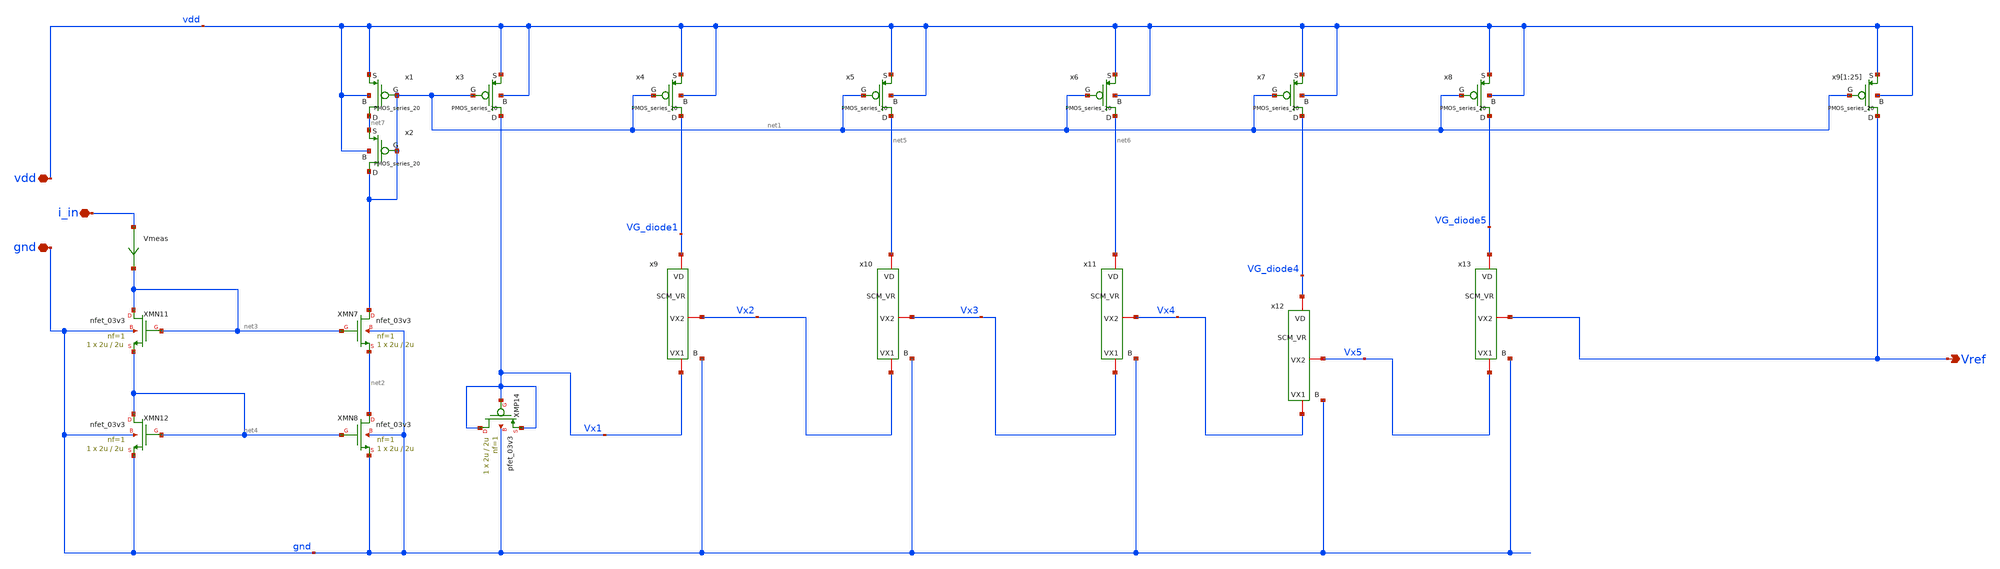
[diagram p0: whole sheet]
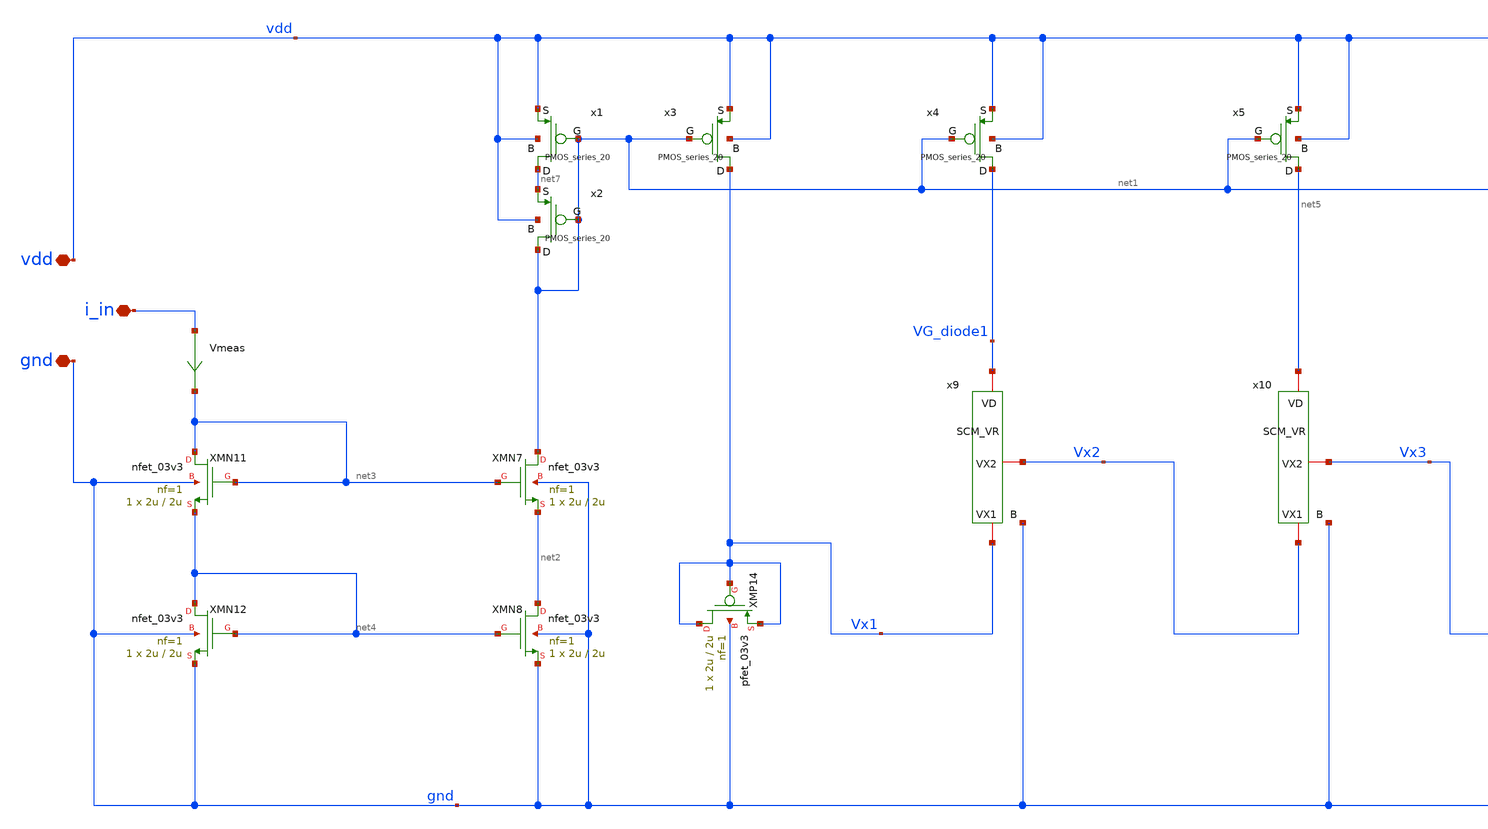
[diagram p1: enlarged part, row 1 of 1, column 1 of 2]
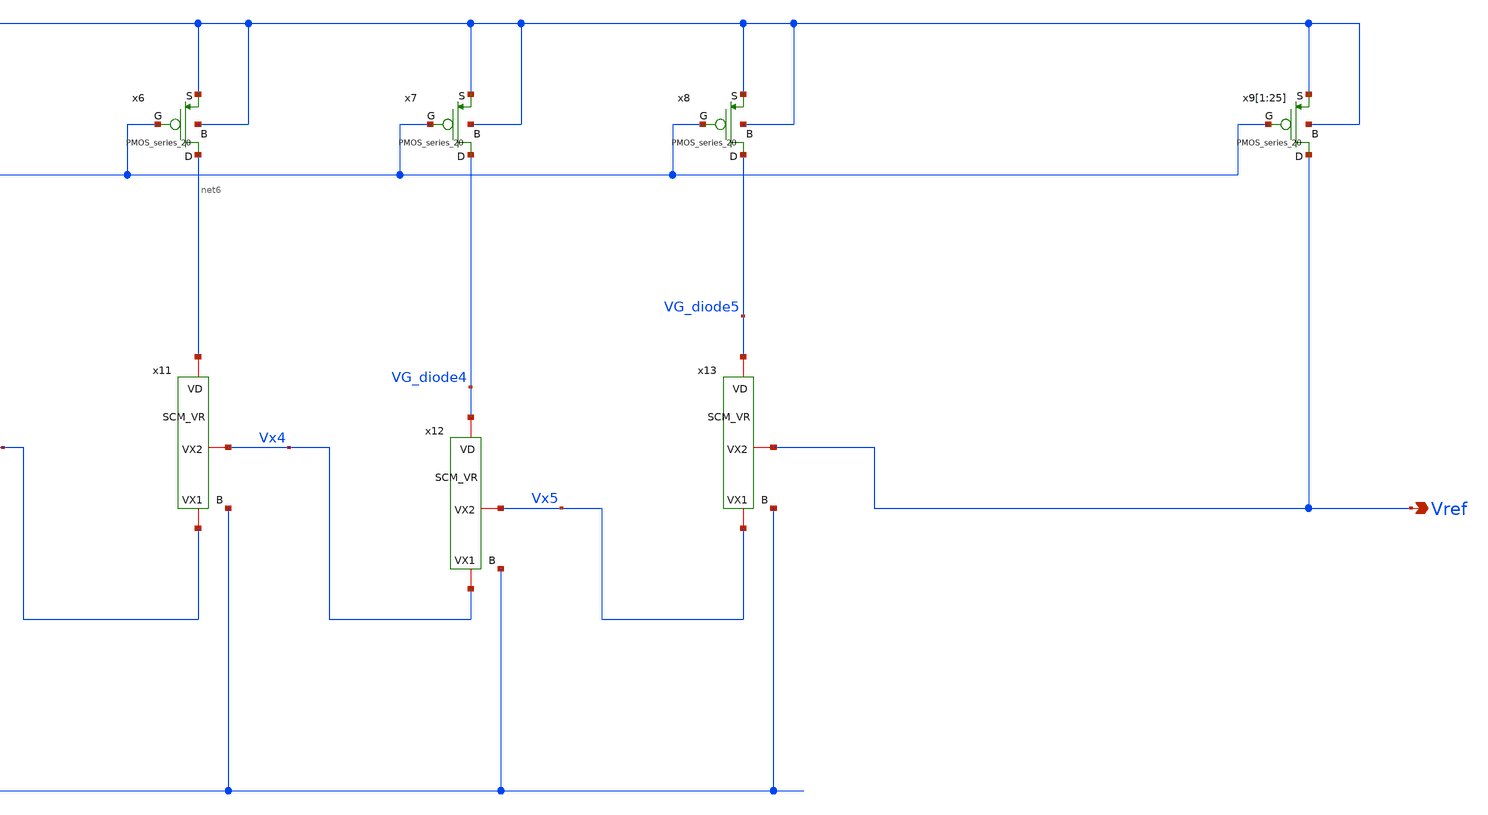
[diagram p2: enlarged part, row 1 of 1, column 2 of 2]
** sch_path: Voltage_Reference/symbols_vr/Voltege_Reference.sch
**.subckt Voltege_Reference i_in vdd gnd Vref
*.iopin i_in
*.iopin vdd
*.iopin gnd
*.opin Vref
XMN7 net1 net3 net2 gnd nfet_03v3 L=2u W=2u nf=1 ad='int((nf+1)/2) * W/nf * 0.18u' as='int((nf+2)/2) * W/nf * 0.18u'
+ pd='2*int((nf+1)/2) * (W/nf + 0.18u)' ps='2*int((nf+2)/2) * (W/nf + 0.18u)' nrd='0.18u / W' nrs='0.18u / W'
+ sa=0 sb=0 sd=0 m=1
XMN8 net2 net4 gnd gnd nfet_03v3 L=2u W=2u nf=1 ad='int((nf+1)/2) * W/nf * 0.18u' as='int((nf+2)/2) * W/nf * 0.18u'
+ pd='2*int((nf+1)/2) * (W/nf + 0.18u)' ps='2*int((nf+2)/2) * (W/nf + 0.18u)' nrd='0.18u / W' nrs='0.18u / W'
+ sa=0 sb=0 sd=0 m=1
XMP14 Vx1 Vx1 Vx1 gnd pfet_03v3 L=2u W=2u nf=1 ad='int((nf+1)/2) * W/nf * 0.18u' as='int((nf+2)/2) * W/nf * 0.18u'
+ pd='2*int((nf+1)/2) * (W/nf + 0.18u)' ps='2*int((nf+2)/2) * (W/nf + 0.18u)' nrd='0.18u / W' nrs='0.18u / W'
+ sa=0 sb=0 sd=0 m=1
XMN11 net3 net3 net4 gnd nfet_03v3 L=2u W=2u nf=1 ad='int((nf+1)/2) * W/nf * 0.18u' as='int((nf+2)/2) * W/nf * 0.18u'
+ pd='2*int((nf+1)/2) * (W/nf + 0.18u)' ps='2*int((nf+2)/2) * (W/nf + 0.18u)' nrd='0.18u / W' nrs='0.18u / W'
+ sa=0 sb=0 sd=0 m=1
XMN12 net4 net4 gnd gnd nfet_03v3 L=2u W=2u nf=1 ad='int((nf+1)/2) * W/nf * 0.18u' as='int((nf+2)/2) * W/nf * 0.18u'
+ pd='2*int((nf+1)/2) * (W/nf + 0.18u)' ps='2*int((nf+2)/2) * (W/nf + 0.18u)' nrd='0.18u / W' nrs='0.18u / W'
+ sa=0 sb=0 sd=0 m=1
Vmeas i_in net3 0
.save i(vmeas)
x1 vdd net7 vdd net1 PMOS_series_20
x2 net7 net1 vdd net1 PMOS_series_20
x3 vdd Vx1 vdd net1 PMOS_series_20
x4 vdd VG_diode1 vdd net1 PMOS_series_20
x5 vdd net5 vdd net1 PMOS_series_20
x6 vdd net6 vdd net1 PMOS_series_20
x7 vdd VG_diode4 vdd net1 PMOS_series_20
x8 vdd VG_diode5 vdd net1 PMOS_series_20
x9[1] vdd Vref vdd net1 PMOS_series_20
x9[2] vdd Vref vdd net1 PMOS_series_20
x9[3] vdd Vref vdd net1 PMOS_series_20
x9[4] vdd Vref vdd net1 PMOS_series_20
x9[5] vdd Vref vdd net1 PMOS_series_20
x9[6] vdd Vref vdd net1 PMOS_series_20
x9[7] vdd Vref vdd net1 PMOS_series_20
x9[8] vdd Vref vdd net1 PMOS_series_20
x9[9] vdd Vref vdd net1 PMOS_series_20
x9[10] vdd Vref vdd net1 PMOS_series_20
x9[11] vdd Vref vdd net1 PMOS_series_20
x9[12] vdd Vref vdd net1 PMOS_series_20
x9[13] vdd Vref vdd net1 PMOS_series_20
x9[14] vdd Vref vdd net1 PMOS_series_20
x9[15] vdd Vref vdd net1 PMOS_series_20
x9[16] vdd Vref vdd net1 PMOS_series_20
x9[17] vdd Vref vdd net1 PMOS_series_20
x9[18] vdd Vref vdd net1 PMOS_series_20
x9[19] vdd Vref vdd net1 PMOS_series_20
x9[20] vdd Vref vdd net1 PMOS_series_20
x9[21] vdd Vref vdd net1 PMOS_series_20
x9[22] vdd Vref vdd net1 PMOS_series_20
x9[23] vdd Vref vdd net1 PMOS_series_20
x9[24] vdd Vref vdd net1 PMOS_series_20
x9[25] vdd Vref vdd net1 PMOS_series_20
x9 VG_diode1 Vx1 Vx2 gnd SCM_VR
x10 net5 Vx2 Vx3 gnd SCM_VR
x11 net6 Vx3 Vx4 gnd SCM_VR
x12 VG_diode4 Vx4 Vx5 gnd SCM_VR
x13 VG_diode5 Vx5 Vref gnd SCM_VR
**.ends

* expanding   symbol:  symbols_vr/PMOS_series_20.sym # of pins=4
** sym_path: Voltage_Reference/symbols_vr/PMOS_series_20.sym
** sch_path: Voltage_Reference/symbols_vr/PMOS_series_20.sch
.subckt PMOS_series_20 S D B G
*.iopin S
*.iopin D
*.iopin B
*.iopin G
XMP1 net1 G S B pfet_03v3 L=2u W=2u nf=1 ad='int((nf+1)/2) * W/nf * 0.18u' as='int((nf+2)/2) * W/nf * 0.18u'
+ pd='2*int((nf+1)/2) * (W/nf + 0.18u)' ps='2*int((nf+2)/2) * (W/nf + 0.18u)' nrd='0.18u / W' nrs='0.18u / W'
+ sa=0 sb=0 sd=0 m=1
XMP2 net3 G net1 B pfet_03v3 L=2u W=2u nf=1 ad='int((nf+1)/2) * W/nf * 0.18u' as='int((nf+2)/2) * W/nf * 0.18u'
+ pd='2*int((nf+1)/2) * (W/nf + 0.18u)' ps='2*int((nf+2)/2) * (W/nf + 0.18u)' nrd='0.18u / W' nrs='0.18u / W'
+ sa=0 sb=0 sd=0 m=1
XMP3 net2 G net3 B pfet_03v3 L=2u W=2u nf=1 ad='int((nf+1)/2) * W/nf * 0.18u' as='int((nf+2)/2) * W/nf * 0.18u'
+ pd='2*int((nf+1)/2) * (W/nf + 0.18u)' ps='2*int((nf+2)/2) * (W/nf + 0.18u)' nrd='0.18u / W' nrs='0.18u / W'
+ sa=0 sb=0 sd=0 m=1
XMP4 net5 G net2 B pfet_03v3 L=2u W=2u nf=1 ad='int((nf+1)/2) * W/nf * 0.18u' as='int((nf+2)/2) * W/nf * 0.18u'
+ pd='2*int((nf+1)/2) * (W/nf + 0.18u)' ps='2*int((nf+2)/2) * (W/nf + 0.18u)' nrd='0.18u / W' nrs='0.18u / W'
+ sa=0 sb=0 sd=0 m=1
XMP5 net4 G net5 B pfet_03v3 L=2u W=2u nf=1 ad='int((nf+1)/2) * W/nf * 0.18u' as='int((nf+2)/2) * W/nf * 0.18u'
+ pd='2*int((nf+1)/2) * (W/nf + 0.18u)' ps='2*int((nf+2)/2) * (W/nf + 0.18u)' nrd='0.18u / W' nrs='0.18u / W'
+ sa=0 sb=0 sd=0 m=1
XMP6 net7 G net4 B pfet_03v3 L=2u W=2u nf=1 ad='int((nf+1)/2) * W/nf * 0.18u' as='int((nf+2)/2) * W/nf * 0.18u'
+ pd='2*int((nf+1)/2) * (W/nf + 0.18u)' ps='2*int((nf+2)/2) * (W/nf + 0.18u)' nrd='0.18u / W' nrs='0.18u / W'
+ sa=0 sb=0 sd=0 m=1
XMP7 net6 G net7 B pfet_03v3 L=2u W=2u nf=1 ad='int((nf+1)/2) * W/nf * 0.18u' as='int((nf+2)/2) * W/nf * 0.18u'
+ pd='2*int((nf+1)/2) * (W/nf + 0.18u)' ps='2*int((nf+2)/2) * (W/nf + 0.18u)' nrd='0.18u / W' nrs='0.18u / W'
+ sa=0 sb=0 sd=0 m=1
XMP8 net9 G net6 B pfet_03v3 L=2u W=2u nf=1 ad='int((nf+1)/2) * W/nf * 0.18u' as='int((nf+2)/2) * W/nf * 0.18u'
+ pd='2*int((nf+1)/2) * (W/nf + 0.18u)' ps='2*int((nf+2)/2) * (W/nf + 0.18u)' nrd='0.18u / W' nrs='0.18u / W'
+ sa=0 sb=0 sd=0 m=1
XMP9 net8 G net9 B pfet_03v3 L=2u W=2u nf=1 ad='int((nf+1)/2) * W/nf * 0.18u' as='int((nf+2)/2) * W/nf * 0.18u'
+ pd='2*int((nf+1)/2) * (W/nf + 0.18u)' ps='2*int((nf+2)/2) * (W/nf + 0.18u)' nrd='0.18u / W' nrs='0.18u / W'
+ sa=0 sb=0 sd=0 m=1
XMP10 net19 G net8 B pfet_03v3 L=2u W=2u nf=1 ad='int((nf+1)/2) * W/nf * 0.18u' as='int((nf+2)/2) * W/nf * 0.18u'
+ pd='2*int((nf+1)/2) * (W/nf + 0.18u)' ps='2*int((nf+2)/2) * (W/nf + 0.18u)' nrd='0.18u / W' nrs='0.18u / W'
+ sa=0 sb=0 sd=0 m=1
XMP11 net10 G net19 B pfet_03v3 L=2u W=2u nf=1 ad='int((nf+1)/2) * W/nf * 0.18u' as='int((nf+2)/2) * W/nf * 0.18u'
+ pd='2*int((nf+1)/2) * (W/nf + 0.18u)' ps='2*int((nf+2)/2) * (W/nf + 0.18u)' nrd='0.18u / W' nrs='0.18u / W'
+ sa=0 sb=0 sd=0 m=1
XMP12 net12 G net10 B pfet_03v3 L=2u W=2u nf=1 ad='int((nf+1)/2) * W/nf * 0.18u' as='int((nf+2)/2) * W/nf * 0.18u'
+ pd='2*int((nf+1)/2) * (W/nf + 0.18u)' ps='2*int((nf+2)/2) * (W/nf + 0.18u)' nrd='0.18u / W' nrs='0.18u / W'
+ sa=0 sb=0 sd=0 m=1
XMP13 net11 G net12 B pfet_03v3 L=2u W=2u nf=1 ad='int((nf+1)/2) * W/nf * 0.18u' as='int((nf+2)/2) * W/nf * 0.18u'
+ pd='2*int((nf+1)/2) * (W/nf + 0.18u)' ps='2*int((nf+2)/2) * (W/nf + 0.18u)' nrd='0.18u / W' nrs='0.18u / W'
+ sa=0 sb=0 sd=0 m=1
XMP14 net14 G net11 B pfet_03v3 L=2u W=2u nf=1 ad='int((nf+1)/2) * W/nf * 0.18u' as='int((nf+2)/2) * W/nf * 0.18u'
+ pd='2*int((nf+1)/2) * (W/nf + 0.18u)' ps='2*int((nf+2)/2) * (W/nf + 0.18u)' nrd='0.18u / W' nrs='0.18u / W'
+ sa=0 sb=0 sd=0 m=1
XMP15 net13 G net14 B pfet_03v3 L=2u W=2u nf=1 ad='int((nf+1)/2) * W/nf * 0.18u' as='int((nf+2)/2) * W/nf * 0.18u'
+ pd='2*int((nf+1)/2) * (W/nf + 0.18u)' ps='2*int((nf+2)/2) * (W/nf + 0.18u)' nrd='0.18u / W' nrs='0.18u / W'
+ sa=0 sb=0 sd=0 m=1
XMP16 net16 G net13 B pfet_03v3 L=2u W=2u nf=1 ad='int((nf+1)/2) * W/nf * 0.18u' as='int((nf+2)/2) * W/nf * 0.18u'
+ pd='2*int((nf+1)/2) * (W/nf + 0.18u)' ps='2*int((nf+2)/2) * (W/nf + 0.18u)' nrd='0.18u / W' nrs='0.18u / W'
+ sa=0 sb=0 sd=0 m=1
XMP17 net15 G net16 B pfet_03v3 L=2u W=2u nf=1 ad='int((nf+1)/2) * W/nf * 0.18u' as='int((nf+2)/2) * W/nf * 0.18u'
+ pd='2*int((nf+1)/2) * (W/nf + 0.18u)' ps='2*int((nf+2)/2) * (W/nf + 0.18u)' nrd='0.18u / W' nrs='0.18u / W'
+ sa=0 sb=0 sd=0 m=1
XMP18 net18 G net15 B pfet_03v3 L=2u W=2u nf=1 ad='int((nf+1)/2) * W/nf * 0.18u' as='int((nf+2)/2) * W/nf * 0.18u'
+ pd='2*int((nf+1)/2) * (W/nf + 0.18u)' ps='2*int((nf+2)/2) * (W/nf + 0.18u)' nrd='0.18u / W' nrs='0.18u / W'
+ sa=0 sb=0 sd=0 m=1
XMP19 net17 G net18 B pfet_03v3 L=2u W=2u nf=1 ad='int((nf+1)/2) * W/nf * 0.18u' as='int((nf+2)/2) * W/nf * 0.18u'
+ pd='2*int((nf+1)/2) * (W/nf + 0.18u)' ps='2*int((nf+2)/2) * (W/nf + 0.18u)' nrd='0.18u / W' nrs='0.18u / W'
+ sa=0 sb=0 sd=0 m=1
XMP20 D G net17 B pfet_03v3 L=2u W=2u nf=1 ad='int((nf+1)/2) * W/nf * 0.18u' as='int((nf+2)/2) * W/nf * 0.18u'
+ pd='2*int((nf+1)/2) * (W/nf + 0.18u)' ps='2*int((nf+2)/2) * (W/nf + 0.18u)' nrd='0.18u / W' nrs='0.18u / W'
+ sa=0 sb=0 sd=0 m=1
XMP21[1] B B B B pfet_03v3 L=2u W=2u nf=1 ad='int((nf+1)/2) * W/nf * 0.18u' as='int((nf+2)/2) * W/nf * 0.18u'
+ pd='2*int((nf+1)/2) * (W/nf + 0.18u)' ps='2*int((nf+2)/2) * (W/nf + 0.18u)' nrd='0.18u / W' nrs='0.18u / W'
+ sa=0 sb=0 sd=0 m=1
XMP21[2] B B B B pfet_03v3 L=2u W=2u nf=1 ad='int((nf+1)/2) * W/nf * 0.18u' as='int((nf+2)/2) * W/nf * 0.18u'
+ pd='2*int((nf+1)/2) * (W/nf + 0.18u)' ps='2*int((nf+2)/2) * (W/nf + 0.18u)' nrd='0.18u / W' nrs='0.18u / W'
+ sa=0 sb=0 sd=0 m=1
XMP21[3] B B B B pfet_03v3 L=2u W=2u nf=1 ad='int((nf+1)/2) * W/nf * 0.18u' as='int((nf+2)/2) * W/nf * 0.18u'
+ pd='2*int((nf+1)/2) * (W/nf + 0.18u)' ps='2*int((nf+2)/2) * (W/nf + 0.18u)' nrd='0.18u / W' nrs='0.18u / W'
+ sa=0 sb=0 sd=0 m=1
XMP21[4] B B B B pfet_03v3 L=2u W=2u nf=1 ad='int((nf+1)/2) * W/nf * 0.18u' as='int((nf+2)/2) * W/nf * 0.18u'
+ pd='2*int((nf+1)/2) * (W/nf + 0.18u)' ps='2*int((nf+2)/2) * (W/nf + 0.18u)' nrd='0.18u / W' nrs='0.18u / W'
+ sa=0 sb=0 sd=0 m=1
XMP21[5] B B B B pfet_03v3 L=2u W=2u nf=1 ad='int((nf+1)/2) * W/nf * 0.18u' as='int((nf+2)/2) * W/nf * 0.18u'
+ pd='2*int((nf+1)/2) * (W/nf + 0.18u)' ps='2*int((nf+2)/2) * (W/nf + 0.18u)' nrd='0.18u / W' nrs='0.18u / W'
+ sa=0 sb=0 sd=0 m=1
XMP21[6] B B B B pfet_03v3 L=2u W=2u nf=1 ad='int((nf+1)/2) * W/nf * 0.18u' as='int((nf+2)/2) * W/nf * 0.18u'
+ pd='2*int((nf+1)/2) * (W/nf + 0.18u)' ps='2*int((nf+2)/2) * (W/nf + 0.18u)' nrd='0.18u / W' nrs='0.18u / W'
+ sa=0 sb=0 sd=0 m=1
XMP21[7] B B B B pfet_03v3 L=2u W=2u nf=1 ad='int((nf+1)/2) * W/nf * 0.18u' as='int((nf+2)/2) * W/nf * 0.18u'
+ pd='2*int((nf+1)/2) * (W/nf + 0.18u)' ps='2*int((nf+2)/2) * (W/nf + 0.18u)' nrd='0.18u / W' nrs='0.18u / W'
+ sa=0 sb=0 sd=0 m=1
XMP21[8] B B B B pfet_03v3 L=2u W=2u nf=1 ad='int((nf+1)/2) * W/nf * 0.18u' as='int((nf+2)/2) * W/nf * 0.18u'
+ pd='2*int((nf+1)/2) * (W/nf + 0.18u)' ps='2*int((nf+2)/2) * (W/nf + 0.18u)' nrd='0.18u / W' nrs='0.18u / W'
+ sa=0 sb=0 sd=0 m=1
XMP21[9] B B B B pfet_03v3 L=2u W=2u nf=1 ad='int((nf+1)/2) * W/nf * 0.18u' as='int((nf+2)/2) * W/nf * 0.18u'
+ pd='2*int((nf+1)/2) * (W/nf + 0.18u)' ps='2*int((nf+2)/2) * (W/nf + 0.18u)' nrd='0.18u / W' nrs='0.18u / W'
+ sa=0 sb=0 sd=0 m=1
XMP21[10] B B B B pfet_03v3 L=2u W=2u nf=1 ad='int((nf+1)/2) * W/nf * 0.18u' as='int((nf+2)/2) * W/nf * 0.18u'
+ pd='2*int((nf+1)/2) * (W/nf + 0.18u)' ps='2*int((nf+2)/2) * (W/nf + 0.18u)' nrd='0.18u / W' nrs='0.18u / W'
+ sa=0 sb=0 sd=0 m=1
XMP21[11] B B B B pfet_03v3 L=2u W=2u nf=1 ad='int((nf+1)/2) * W/nf * 0.18u' as='int((nf+2)/2) * W/nf * 0.18u'
+ pd='2*int((nf+1)/2) * (W/nf + 0.18u)' ps='2*int((nf+2)/2) * (W/nf + 0.18u)' nrd='0.18u / W' nrs='0.18u / W'
+ sa=0 sb=0 sd=0 m=1
XMP21[12] B B B B pfet_03v3 L=2u W=2u nf=1 ad='int((nf+1)/2) * W/nf * 0.18u' as='int((nf+2)/2) * W/nf * 0.18u'
+ pd='2*int((nf+1)/2) * (W/nf + 0.18u)' ps='2*int((nf+2)/2) * (W/nf + 0.18u)' nrd='0.18u / W' nrs='0.18u / W'
+ sa=0 sb=0 sd=0 m=1
XMP21[13] B B B B pfet_03v3 L=2u W=2u nf=1 ad='int((nf+1)/2) * W/nf * 0.18u' as='int((nf+2)/2) * W/nf * 0.18u'
+ pd='2*int((nf+1)/2) * (W/nf + 0.18u)' ps='2*int((nf+2)/2) * (W/nf + 0.18u)' nrd='0.18u / W' nrs='0.18u / W'
+ sa=0 sb=0 sd=0 m=1
XMP21[14] B B B B pfet_03v3 L=2u W=2u nf=1 ad='int((nf+1)/2) * W/nf * 0.18u' as='int((nf+2)/2) * W/nf * 0.18u'
+ pd='2*int((nf+1)/2) * (W/nf + 0.18u)' ps='2*int((nf+2)/2) * (W/nf + 0.18u)' nrd='0.18u / W' nrs='0.18u / W'
+ sa=0 sb=0 sd=0 m=1
XMP21[15] B B B B pfet_03v3 L=2u W=2u nf=1 ad='int((nf+1)/2) * W/nf * 0.18u' as='int((nf+2)/2) * W/nf * 0.18u'
+ pd='2*int((nf+1)/2) * (W/nf + 0.18u)' ps='2*int((nf+2)/2) * (W/nf + 0.18u)' nrd='0.18u / W' nrs='0.18u / W'
+ sa=0 sb=0 sd=0 m=1
XMP21[16] B B B B pfet_03v3 L=2u W=2u nf=1 ad='int((nf+1)/2) * W/nf * 0.18u' as='int((nf+2)/2) * W/nf * 0.18u'
+ pd='2*int((nf+1)/2) * (W/nf + 0.18u)' ps='2*int((nf+2)/2) * (W/nf + 0.18u)' nrd='0.18u / W' nrs='0.18u / W'
+ sa=0 sb=0 sd=0 m=1
XMP21[17] B B B B pfet_03v3 L=2u W=2u nf=1 ad='int((nf+1)/2) * W/nf * 0.18u' as='int((nf+2)/2) * W/nf * 0.18u'
+ pd='2*int((nf+1)/2) * (W/nf + 0.18u)' ps='2*int((nf+2)/2) * (W/nf + 0.18u)' nrd='0.18u / W' nrs='0.18u / W'
+ sa=0 sb=0 sd=0 m=1
XMP21[18] B B B B pfet_03v3 L=2u W=2u nf=1 ad='int((nf+1)/2) * W/nf * 0.18u' as='int((nf+2)/2) * W/nf * 0.18u'
+ pd='2*int((nf+1)/2) * (W/nf + 0.18u)' ps='2*int((nf+2)/2) * (W/nf + 0.18u)' nrd='0.18u / W' nrs='0.18u / W'
+ sa=0 sb=0 sd=0 m=1
XMP21[19] B B B B pfet_03v3 L=2u W=2u nf=1 ad='int((nf+1)/2) * W/nf * 0.18u' as='int((nf+2)/2) * W/nf * 0.18u'
+ pd='2*int((nf+1)/2) * (W/nf + 0.18u)' ps='2*int((nf+2)/2) * (W/nf + 0.18u)' nrd='0.18u / W' nrs='0.18u / W'
+ sa=0 sb=0 sd=0 m=1
XMP21[20] B B B B pfet_03v3 L=2u W=2u nf=1 ad='int((nf+1)/2) * W/nf * 0.18u' as='int((nf+2)/2) * W/nf * 0.18u'
+ pd='2*int((nf+1)/2) * (W/nf + 0.18u)' ps='2*int((nf+2)/2) * (W/nf + 0.18u)' nrd='0.18u / W' nrs='0.18u / W'
+ sa=0 sb=0 sd=0 m=1
XMP21[21] B B B B pfet_03v3 L=2u W=2u nf=1 ad='int((nf+1)/2) * W/nf * 0.18u' as='int((nf+2)/2) * W/nf * 0.18u'
+ pd='2*int((nf+1)/2) * (W/nf + 0.18u)' ps='2*int((nf+2)/2) * (W/nf + 0.18u)' nrd='0.18u / W' nrs='0.18u / W'
+ sa=0 sb=0 sd=0 m=1
XMP21[22] B B B B pfet_03v3 L=2u W=2u nf=1 ad='int((nf+1)/2) * W/nf * 0.18u' as='int((nf+2)/2) * W/nf * 0.18u'
+ pd='2*int((nf+1)/2) * (W/nf + 0.18u)' ps='2*int((nf+2)/2) * (W/nf + 0.18u)' nrd='0.18u / W' nrs='0.18u / W'
+ sa=0 sb=0 sd=0 m=1
XMP21[23] B B B B pfet_03v3 L=2u W=2u nf=1 ad='int((nf+1)/2) * W/nf * 0.18u' as='int((nf+2)/2) * W/nf * 0.18u'
+ pd='2*int((nf+1)/2) * (W/nf + 0.18u)' ps='2*int((nf+2)/2) * (W/nf + 0.18u)' nrd='0.18u / W' nrs='0.18u / W'
+ sa=0 sb=0 sd=0 m=1
XMP21[24] B B B B pfet_03v3 L=2u W=2u nf=1 ad='int((nf+1)/2) * W/nf * 0.18u' as='int((nf+2)/2) * W/nf * 0.18u'
+ pd='2*int((nf+1)/2) * (W/nf + 0.18u)' ps='2*int((nf+2)/2) * (W/nf + 0.18u)' nrd='0.18u / W' nrs='0.18u / W'
+ sa=0 sb=0 sd=0 m=1
XMP21[25] B B B B pfet_03v3 L=2u W=2u nf=1 ad='int((nf+1)/2) * W/nf * 0.18u' as='int((nf+2)/2) * W/nf * 0.18u'
+ pd='2*int((nf+1)/2) * (W/nf + 0.18u)' ps='2*int((nf+2)/2) * (W/nf + 0.18u)' nrd='0.18u / W' nrs='0.18u / W'
+ sa=0 sb=0 sd=0 m=1
.ends


* expanding   symbol:  symbols_vr/SCM_VR.sym # of pins=4
** sym_path: Voltage_Reference/symbols_vr/SCM_VR.sym
** sch_path: Voltage_Reference/symbols_vr/SCM_VR.sch
.subckt SCM_VR VD VX1 VX2 B
*.iopin VD
*.iopin VX1
*.iopin VX2
*.iopin B
XMN1[1] VD VD VX2 B nfet_03v3 L=2u W=2u nf=1 ad='int((nf+1)/2) * W/nf * 0.18u' as='int((nf+2)/2) * W/nf * 0.18u'
+ pd='2*int((nf+1)/2) * (W/nf + 0.18u)' ps='2*int((nf+2)/2) * (W/nf + 0.18u)' nrd='0.18u / W' nrs='0.18u / W'
+ sa=0 sb=0 sd=0 m=1
XMN1[2] VD VD VX2 B nfet_03v3 L=2u W=2u nf=1 ad='int((nf+1)/2) * W/nf * 0.18u' as='int((nf+2)/2) * W/nf * 0.18u'
+ pd='2*int((nf+1)/2) * (W/nf + 0.18u)' ps='2*int((nf+2)/2) * (W/nf + 0.18u)' nrd='0.18u / W' nrs='0.18u / W'
+ sa=0 sb=0 sd=0 m=1
XMN1[3] VD VD VX2 B nfet_03v3 L=2u W=2u nf=1 ad='int((nf+1)/2) * W/nf * 0.18u' as='int((nf+2)/2) * W/nf * 0.18u'
+ pd='2*int((nf+1)/2) * (W/nf + 0.18u)' ps='2*int((nf+2)/2) * (W/nf + 0.18u)' nrd='0.18u / W' nrs='0.18u / W'
+ sa=0 sb=0 sd=0 m=1
XMN1[4] VD VD VX2 B nfet_03v3 L=2u W=2u nf=1 ad='int((nf+1)/2) * W/nf * 0.18u' as='int((nf+2)/2) * W/nf * 0.18u'
+ pd='2*int((nf+1)/2) * (W/nf + 0.18u)' ps='2*int((nf+2)/2) * (W/nf + 0.18u)' nrd='0.18u / W' nrs='0.18u / W'
+ sa=0 sb=0 sd=0 m=1
XMN1[5] VD VD VX2 B nfet_03v3 L=2u W=2u nf=1 ad='int((nf+1)/2) * W/nf * 0.18u' as='int((nf+2)/2) * W/nf * 0.18u'
+ pd='2*int((nf+1)/2) * (W/nf + 0.18u)' ps='2*int((nf+2)/2) * (W/nf + 0.18u)' nrd='0.18u / W' nrs='0.18u / W'
+ sa=0 sb=0 sd=0 m=1
XMN2 VX2 VD VX1 B nfet_03v3 L=2u W=2u nf=1 ad='int((nf+1)/2) * W/nf * 0.18u' as='int((nf+2)/2) * W/nf * 0.18u'
+ pd='2*int((nf+1)/2) * (W/nf + 0.18u)' ps='2*int((nf+2)/2) * (W/nf + 0.18u)' nrd='0.18u / W' nrs='0.18u / W'
+ sa=0 sb=0 sd=0 m=1
XMN2[1] B B B B nfet_03v3 L=2u W=2u nf=1 ad='int((nf+1)/2) * W/nf * 0.18u' as='int((nf+2)/2) * W/nf * 0.18u'
+ pd='2*int((nf+1)/2) * (W/nf + 0.18u)' ps='2*int((nf+2)/2) * (W/nf + 0.18u)' nrd='0.18u / W' nrs='0.18u / W'
+ sa=0 sb=0 sd=0 m=1
XMN2[2] B B B B nfet_03v3 L=2u W=2u nf=1 ad='int((nf+1)/2) * W/nf * 0.18u' as='int((nf+2)/2) * W/nf * 0.18u'
+ pd='2*int((nf+1)/2) * (W/nf + 0.18u)' ps='2*int((nf+2)/2) * (W/nf + 0.18u)' nrd='0.18u / W' nrs='0.18u / W'
+ sa=0 sb=0 sd=0 m=1
XMN2[3] B B B B nfet_03v3 L=2u W=2u nf=1 ad='int((nf+1)/2) * W/nf * 0.18u' as='int((nf+2)/2) * W/nf * 0.18u'
+ pd='2*int((nf+1)/2) * (W/nf + 0.18u)' ps='2*int((nf+2)/2) * (W/nf + 0.18u)' nrd='0.18u / W' nrs='0.18u / W'
+ sa=0 sb=0 sd=0 m=1
XMN2[4] B B B B nfet_03v3 L=2u W=2u nf=1 ad='int((nf+1)/2) * W/nf * 0.18u' as='int((nf+2)/2) * W/nf * 0.18u'
+ pd='2*int((nf+1)/2) * (W/nf + 0.18u)' ps='2*int((nf+2)/2) * (W/nf + 0.18u)' nrd='0.18u / W' nrs='0.18u / W'
+ sa=0 sb=0 sd=0 m=1
XMN2[5] B B B B nfet_03v3 L=2u W=2u nf=1 ad='int((nf+1)/2) * W/nf * 0.18u' as='int((nf+2)/2) * W/nf * 0.18u'
+ pd='2*int((nf+1)/2) * (W/nf + 0.18u)' ps='2*int((nf+2)/2) * (W/nf + 0.18u)' nrd='0.18u / W' nrs='0.18u / W'
+ sa=0 sb=0 sd=0 m=1
XMN2[6] B B B B nfet_03v3 L=2u W=2u nf=1 ad='int((nf+1)/2) * W/nf * 0.18u' as='int((nf+2)/2) * W/nf * 0.18u'
+ pd='2*int((nf+1)/2) * (W/nf + 0.18u)' ps='2*int((nf+2)/2) * (W/nf + 0.18u)' nrd='0.18u / W' nrs='0.18u / W'
+ sa=0 sb=0 sd=0 m=1
XMN2[7] B B B B nfet_03v3 L=2u W=2u nf=1 ad='int((nf+1)/2) * W/nf * 0.18u' as='int((nf+2)/2) * W/nf * 0.18u'
+ pd='2*int((nf+1)/2) * (W/nf + 0.18u)' ps='2*int((nf+2)/2) * (W/nf + 0.18u)' nrd='0.18u / W' nrs='0.18u / W'
+ sa=0 sb=0 sd=0 m=1
XMN2[8] B B B B nfet_03v3 L=2u W=2u nf=1 ad='int((nf+1)/2) * W/nf * 0.18u' as='int((nf+2)/2) * W/nf * 0.18u'
+ pd='2*int((nf+1)/2) * (W/nf + 0.18u)' ps='2*int((nf+2)/2) * (W/nf + 0.18u)' nrd='0.18u / W' nrs='0.18u / W'
+ sa=0 sb=0 sd=0 m=1
XMN2[9] B B B B nfet_03v3 L=2u W=2u nf=1 ad='int((nf+1)/2) * W/nf * 0.18u' as='int((nf+2)/2) * W/nf * 0.18u'
+ pd='2*int((nf+1)/2) * (W/nf + 0.18u)' ps='2*int((nf+2)/2) * (W/nf + 0.18u)' nrd='0.18u / W' nrs='0.18u / W'
+ sa=0 sb=0 sd=0 m=1
XMN2[10] B B B B nfet_03v3 L=2u W=2u nf=1 ad='int((nf+1)/2) * W/nf * 0.18u' as='int((nf+2)/2) * W/nf * 0.18u'
+ pd='2*int((nf+1)/2) * (W/nf + 0.18u)' ps='2*int((nf+2)/2) * (W/nf + 0.18u)' nrd='0.18u / W' nrs='0.18u / W'
+ sa=0 sb=0 sd=0 m=1
XMN2[11] B B B B nfet_03v3 L=2u W=2u nf=1 ad='int((nf+1)/2) * W/nf * 0.18u' as='int((nf+2)/2) * W/nf * 0.18u'
+ pd='2*int((nf+1)/2) * (W/nf + 0.18u)' ps='2*int((nf+2)/2) * (W/nf + 0.18u)' nrd='0.18u / W' nrs='0.18u / W'
+ sa=0 sb=0 sd=0 m=1
XMN2[12] B B B B nfet_03v3 L=2u W=2u nf=1 ad='int((nf+1)/2) * W/nf * 0.18u' as='int((nf+2)/2) * W/nf * 0.18u'
+ pd='2*int((nf+1)/2) * (W/nf + 0.18u)' ps='2*int((nf+2)/2) * (W/nf + 0.18u)' nrd='0.18u / W' nrs='0.18u / W'
+ sa=0 sb=0 sd=0 m=1
XMN2[13] B B B B nfet_03v3 L=2u W=2u nf=1 ad='int((nf+1)/2) * W/nf * 0.18u' as='int((nf+2)/2) * W/nf * 0.18u'
+ pd='2*int((nf+1)/2) * (W/nf + 0.18u)' ps='2*int((nf+2)/2) * (W/nf + 0.18u)' nrd='0.18u / W' nrs='0.18u / W'
+ sa=0 sb=0 sd=0 m=1
XMN2[14] B B B B nfet_03v3 L=2u W=2u nf=1 ad='int((nf+1)/2) * W/nf * 0.18u' as='int((nf+2)/2) * W/nf * 0.18u'
+ pd='2*int((nf+1)/2) * (W/nf + 0.18u)' ps='2*int((nf+2)/2) * (W/nf + 0.18u)' nrd='0.18u / W' nrs='0.18u / W'
+ sa=0 sb=0 sd=0 m=1
XMN2[15] B B B B nfet_03v3 L=2u W=2u nf=1 ad='int((nf+1)/2) * W/nf * 0.18u' as='int((nf+2)/2) * W/nf * 0.18u'
+ pd='2*int((nf+1)/2) * (W/nf + 0.18u)' ps='2*int((nf+2)/2) * (W/nf + 0.18u)' nrd='0.18u / W' nrs='0.18u / W'
+ sa=0 sb=0 sd=0 m=1
XMN2[16] B B B B nfet_03v3 L=2u W=2u nf=1 ad='int((nf+1)/2) * W/nf * 0.18u' as='int((nf+2)/2) * W/nf * 0.18u'
+ pd='2*int((nf+1)/2) * (W/nf + 0.18u)' ps='2*int((nf+2)/2) * (W/nf + 0.18u)' nrd='0.18u / W' nrs='0.18u / W'
+ sa=0 sb=0 sd=0 m=1
XMN2[17] B B B B nfet_03v3 L=2u W=2u nf=1 ad='int((nf+1)/2) * W/nf * 0.18u' as='int((nf+2)/2) * W/nf * 0.18u'
+ pd='2*int((nf+1)/2) * (W/nf + 0.18u)' ps='2*int((nf+2)/2) * (W/nf + 0.18u)' nrd='0.18u / W' nrs='0.18u / W'
+ sa=0 sb=0 sd=0 m=1
XMN2[18] B B B B nfet_03v3 L=2u W=2u nf=1 ad='int((nf+1)/2) * W/nf * 0.18u' as='int((nf+2)/2) * W/nf * 0.18u'
+ pd='2*int((nf+1)/2) * (W/nf + 0.18u)' ps='2*int((nf+2)/2) * (W/nf + 0.18u)' nrd='0.18u / W' nrs='0.18u / W'
+ sa=0 sb=0 sd=0 m=1
.ends

.end
